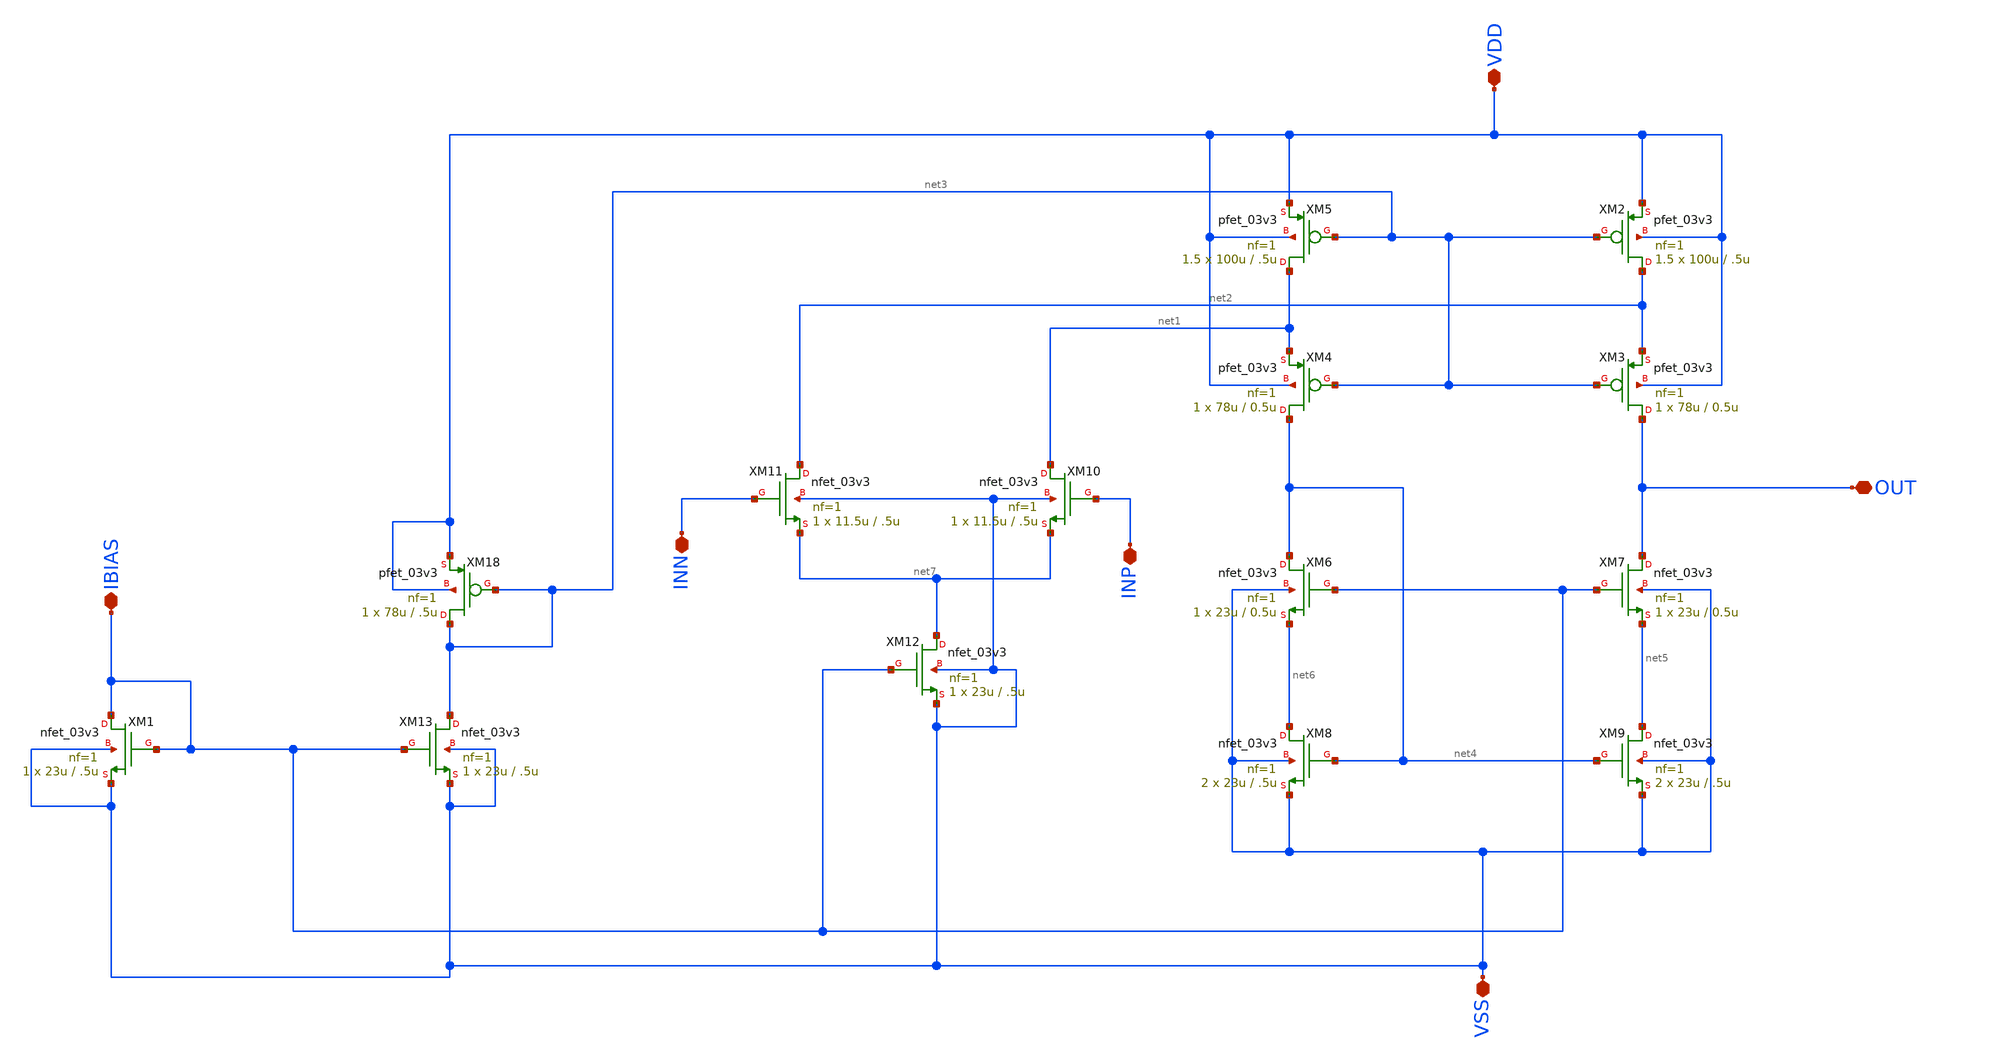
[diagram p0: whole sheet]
** sch_path: designs/libs/core_amps/ota_folded_cascode/symbol_from.sch
**.subckt symbol_from IBIAS INN INP OUT VSS VDD
*.iopin IBIAS
*.iopin INN
*.iopin INP
*.iopin OUT
*.iopin VSS
*.iopin VDD
XM1 IBIAS IBIAS VSS VSS nfet_03v3 L=.5u W=23u nf=1 ad='int((nf+1)/2) * W/nf * 0.18u' as='int((nf+2)/2) * W/nf * 0.18u'
+ pd='2*int((nf+1)/2) * (W/nf + 0.18u)' ps='2*int((nf+2)/2) * (W/nf + 0.18u)' nrd='0.18u / W' nrs='0.18u / W'
+ sa=0 sb=0 sd=0 m=1
XM2 net2 net3 VDD VDD pfet_03v3 L=.5u W=100u nf=1 ad='int((nf+1)/2) * W/nf * 0.18u' as='int((nf+2)/2) * W/nf * 0.18u'
+ pd='2*int((nf+1)/2) * (W/nf + 0.18u)' ps='2*int((nf+2)/2) * (W/nf + 0.18u)' nrd='0.18u / W' nrs='0.18u / W'
+ sa=0 sb=0 sd=0 m=1.5
XM3 OUT net3 net2 VDD pfet_03v3 L=0.5u W=78u nf=1 ad='int((nf+1)/2) * W/nf * 0.18u' as='int((nf+2)/2) * W/nf * 0.18u'
+ pd='2*int((nf+1)/2) * (W/nf + 0.18u)' ps='2*int((nf+2)/2) * (W/nf + 0.18u)' nrd='0.18u / W' nrs='0.18u / W'
+ sa=0 sb=0 sd=0 m=1
XM4 net4 net3 net1 VDD pfet_03v3 L=0.5u W=78u nf=1 ad='int((nf+1)/2) * W/nf * 0.18u' as='int((nf+2)/2) * W/nf * 0.18u'
+ pd='2*int((nf+1)/2) * (W/nf + 0.18u)' ps='2*int((nf+2)/2) * (W/nf + 0.18u)' nrd='0.18u / W' nrs='0.18u / W'
+ sa=0 sb=0 sd=0 m=1
XM5 net1 net3 VDD VDD pfet_03v3 L=.5u W=100u nf=1 ad='int((nf+1)/2) * W/nf * 0.18u' as='int((nf+2)/2) * W/nf * 0.18u'
+ pd='2*int((nf+1)/2) * (W/nf + 0.18u)' ps='2*int((nf+2)/2) * (W/nf + 0.18u)' nrd='0.18u / W' nrs='0.18u / W'
+ sa=0 sb=0 sd=0 m=1.5
XM6 net4 IBIAS net6 VSS nfet_03v3 L=0.5u W=23u nf=1 ad='int((nf+1)/2) * W/nf * 0.18u' as='int((nf+2)/2) * W/nf * 0.18u'
+ pd='2*int((nf+1)/2) * (W/nf + 0.18u)' ps='2*int((nf+2)/2) * (W/nf + 0.18u)' nrd='0.18u / W' nrs='0.18u / W'
+ sa=0 sb=0 sd=0 m=1
XM7 OUT IBIAS net5 VSS nfet_03v3 L=0.5u W=23u nf=1 ad='int((nf+1)/2) * W/nf * 0.18u' as='int((nf+2)/2) * W/nf * 0.18u'
+ pd='2*int((nf+1)/2) * (W/nf + 0.18u)' ps='2*int((nf+2)/2) * (W/nf + 0.18u)' nrd='0.18u / W' nrs='0.18u / W'
+ sa=0 sb=0 sd=0 m=1
XM8 net6 net4 VSS VSS nfet_03v3 L=.5u W=23u nf=1 ad='int((nf+1)/2) * W/nf * 0.18u' as='int((nf+2)/2) * W/nf * 0.18u'
+ pd='2*int((nf+1)/2) * (W/nf + 0.18u)' ps='2*int((nf+2)/2) * (W/nf + 0.18u)' nrd='0.18u / W' nrs='0.18u / W'
+ sa=0 sb=0 sd=0 m=2
XM9 net5 net4 VSS VSS nfet_03v3 L=.5u W=23u nf=1 ad='int((nf+1)/2) * W/nf * 0.18u' as='int((nf+2)/2) * W/nf * 0.18u'
+ pd='2*int((nf+1)/2) * (W/nf + 0.18u)' ps='2*int((nf+2)/2) * (W/nf + 0.18u)' nrd='0.18u / W' nrs='0.18u / W'
+ sa=0 sb=0 sd=0 m=2
XM10 net1 INP net7 VSS nfet_03v3 L=.5u W=11.5u nf=1 ad='int((nf+1)/2) * W/nf * 0.18u' as='int((nf+2)/2) * W/nf * 0.18u'
+ pd='2*int((nf+1)/2) * (W/nf + 0.18u)' ps='2*int((nf+2)/2) * (W/nf + 0.18u)' nrd='0.18u / W' nrs='0.18u / W'
+ sa=0 sb=0 sd=0 m=1
XM12 net7 IBIAS VSS VSS nfet_03v3 L=.5u W=23u nf=1 ad='int((nf+1)/2) * W/nf * 0.18u' as='int((nf+2)/2) * W/nf * 0.18u'
+ pd='2*int((nf+1)/2) * (W/nf + 0.18u)' ps='2*int((nf+2)/2) * (W/nf + 0.18u)' nrd='0.18u / W' nrs='0.18u / W'
+ sa=0 sb=0 sd=0 m=1
XM18 net3 net3 VDD VDD pfet_03v3 L=.5u W=78u nf=1 ad='int((nf+1)/2) * W/nf * 0.18u' as='int((nf+2)/2) * W/nf * 0.18u'
+ pd='2*int((nf+1)/2) * (W/nf + 0.18u)' ps='2*int((nf+2)/2) * (W/nf + 0.18u)' nrd='0.18u / W' nrs='0.18u / W'
+ sa=0 sb=0 sd=0 m=1
XM11 net2 INN net7 VSS nfet_03v3 L=.5u W=11.5u nf=1 ad='int((nf+1)/2) * W/nf * 0.18u' as='int((nf+2)/2) * W/nf * 0.18u'
+ pd='2*int((nf+1)/2) * (W/nf + 0.18u)' ps='2*int((nf+2)/2) * (W/nf + 0.18u)' nrd='0.18u / W' nrs='0.18u / W'
+ sa=0 sb=0 sd=0 m=1
XM13 net3 IBIAS VSS VSS nfet_03v3 L=.5u W=23u nf=1 ad='int((nf+1)/2) * W/nf * 0.18u' as='int((nf+2)/2) * W/nf * 0.18u'
+ pd='2*int((nf+1)/2) * (W/nf + 0.18u)' ps='2*int((nf+2)/2) * (W/nf + 0.18u)' nrd='0.18u / W' nrs='0.18u / W'
+ sa=0 sb=0 sd=0 m=1
**.ends
.end
